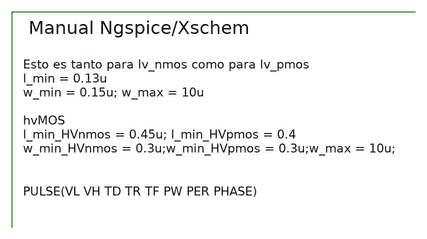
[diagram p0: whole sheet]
** sch_path: xschem/Manual_Instrucciones/Manual_Ngspice_Xschem.sch
**.subckt Manual_Ngspice_Xschem
**** begin user architecture code


.lib cornerMOShv.lib mos_tt
.lib cornerMOSlv.lib mos_tt
*.lib cornerMOShv.lib mos_ff
*.lib cornerMOSlv.lib mos_ff
*.lib cornerMOShv.lib mos_ss
*.lib cornerMOSlv.lib mos_ss
*.lib cornerMOShv.lib mos_sf
*.lib cornerMOSlv.lib mos_sf
*.lib cornerMOShv.lib mos_fs
*.lib cornerMOSlv.lib mos_fs

*.include /opt/pdks/ihp-sg13g2/libs.ref/sg13g2_stdcell/spice/sg13g2_stdcell.spice
*.lib $::SG13G2_MODELS/cornerRES.lib res_typ
*.lib $::SG13G2_MODELS/cornerCAP.lib cap_typ
*.lib $::SG13G2_MODELS/diodes.lib




.option KLU
*.option itl4=100
.option method=gear
*.option maxord=2
*.option trtol=25
*.option lvltim=1
*.option tnum=1e9
*.option reltol=1e-3
*.option abstol=1e-10
*.option vntol=1e-4
*.option event
*.option gmin=1e-10
.option cshunt=1e-13


**** end user architecture code
**.ends
.end
